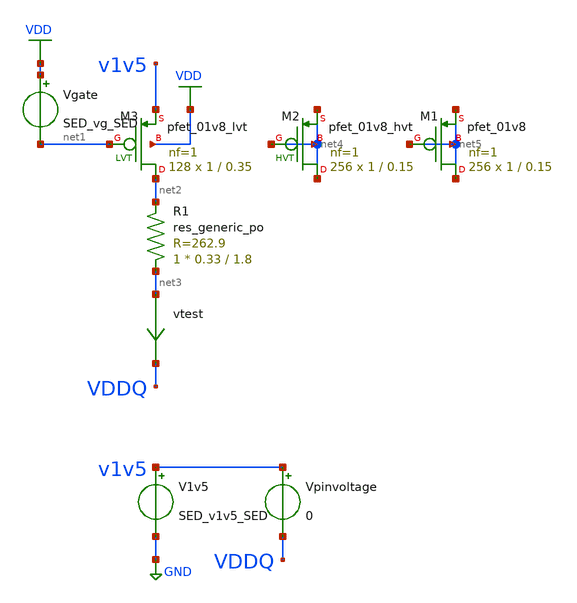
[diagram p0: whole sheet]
** sch_path: test_pu_res.sch
* Copyright 2021 Stefan Frederik Schippers
* Licensed under the Apache License, Version 2.0 (the "License");
* you may not use this file except in compliance with the License.
* You may obtain a copy of the License at
* https://www.apache.org/licenses/LICENSE-2.0
* Unless required by applicable law or agreed to in writing, software
* distributed under the License is distributed on an "AS IS" BASIS,
* WITHOUT WARRANTIES OR CONDITIONS OF ANY KIND, either express or implied.
* See the License for the specific language governing permissions and
* limitations under the License.
**.subckt test_pu_res
Vgate VDD net1 SED_vg_SED
XR1 net3 net2 sky130_fd_pr__res_generic_po W=0.33 L=1.8 m=1
vtest net3 VDDQ 0
.save i(vtest)
XM2 net4 net4 net4 net4 sky130_fd_pr__pfet_01v8_hvt L=0.15 W=1 nf=1 ad='int((nf+1)/2) * W/nf * 0.29'
+ as='int((nf+2)/2) * W/nf * 0.29' pd='2*int((nf+1)/2) * (W/nf + 0.29)' ps='2*int((nf+2)/2) * (W/nf + 0.29)'
+ nrd='0.29 / W' nrs='0.29 / W' sa=0 sb=0 sd=0 mult=256 m=256
V1v5 v1v5 GND SED_v1v5_SED
Vpinvoltage v1v5 VDDQ 0
XM1 net5 net5 net5 net5 sky130_fd_pr__pfet_01v8 L=0.15 W=1 nf=1 ad='int((nf+1)/2) * W/nf * 0.29' as='int((nf+2)/2) * W/nf * 0.29'
+ pd='2*int((nf+1)/2) * (W/nf + 0.29)' ps='2*int((nf+2)/2) * (W/nf + 0.29)' nrd='0.29 / W' nrs='0.29 / W'
+ sa=0 sb=0 sd=0 mult=256 m=256
XM3 net2 net1 v1v5 VDD sky130_fd_pr__pfet_01v8_lvt L=0.35 W=1 nf=1 ad='int((nf+1)/2) * W/nf * 0.29' as='int((nf+2)/2) * W/nf * 0.29'
+ pd='2*int((nf+1)/2) * (W/nf + 0.29)' ps='2*int((nf+2)/2) * (W/nf + 0.29)' nrd='0.29 / W' nrs='0.29 / W'
+ sa=0 sb=0 sd=0 mult=128 m=128
**** begin user architecture code
 ** Local library links to pdk
.lib ./libs/SED_process_SED_lib.spice SED_process_SED

**** end user architecture code
**.ends
.GLOBAL VDD
.GLOBAL GND
**** begin user architecture code



* power voltage
vvdd VDD 0 1.8

*.param rwidth=4.6

.control
save all
set temp=SED_temp_SED

* RUN SIMULATION
dc Vpinvoltage 0.3 1.2 0.05
* OUTPUT
print (SED_v1v5_SED-vddq)/i(vtest)
wrdata out/data/SED_plotName_SED.txt (SED_v1v5_SED-vddq)/i(vtest)
set hcopydevtype = svg
hardcopy ./out/plots/SED_plotName_SED.svg (SED_v1v5_SED-vddq)/I(vtest) vs vddq title 'Resistance vs pin voltage'

.endc


**** end user architecture code
.end
